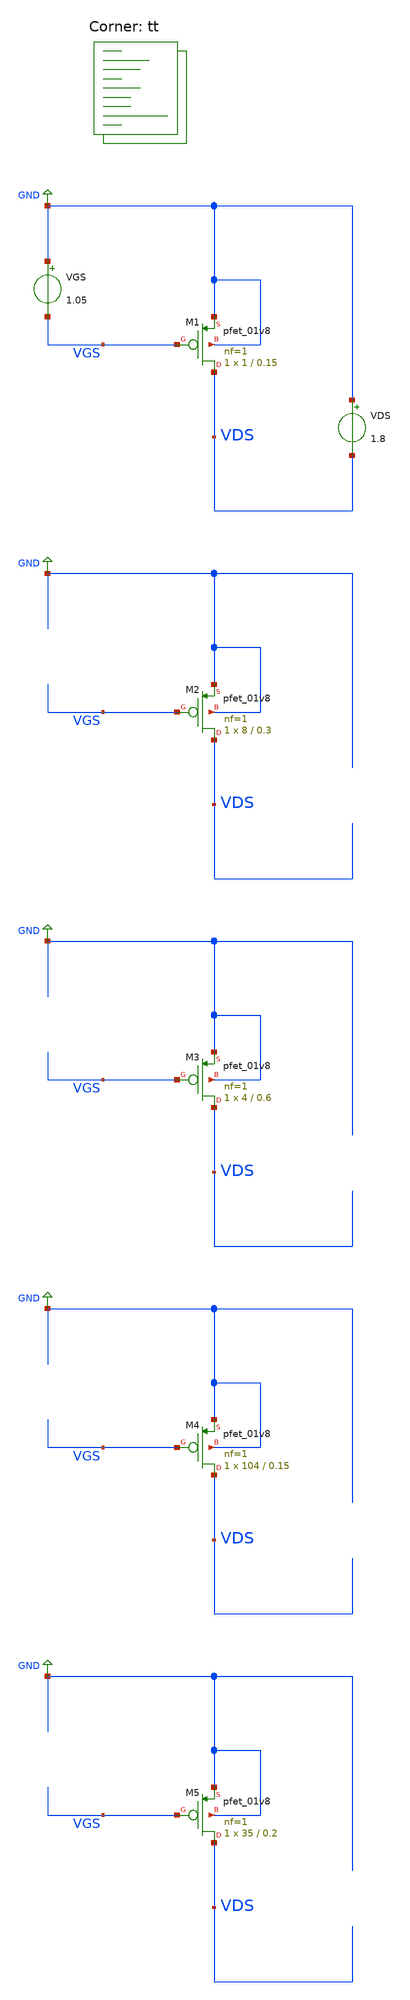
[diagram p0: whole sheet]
** sch_path: projects/opamp/xschem_ngspice/vds_vgs_sweep_pfet.sch
**.subckt vds_vgs_sweep_pfet
VGS GND VGS 1.05
VDS GND VDS 1.8
XM1 VDS VGS GND GND sky130_fd_pr__pfet_01v8 L=0.15 W=1 nf=1 ad='int((nf+1)/2) * W/nf * 0.29' as='int((nf+2)/2) * W/nf * 0.29'
+ pd='2*int((nf+1)/2) * (W/nf + 0.29)' ps='2*int((nf+2)/2) * (W/nf + 0.29)' nrd='0.29 / W' nrs='0.29 / W'
+ sa=0 sb=0 sd=0 mult=1 m=1
XM3 VDS VGS GND GND sky130_fd_pr__pfet_01v8 L=0.6 W=4 nf=1 ad='int((nf+1)/2) * W/nf * 0.29' as='int((nf+2)/2) * W/nf * 0.29'
+ pd='2*int((nf+1)/2) * (W/nf + 0.29)' ps='2*int((nf+2)/2) * (W/nf + 0.29)' nrd='0.29 / W' nrs='0.29 / W'
+ sa=0 sb=0 sd=0 mult=1 m=1
XM2 VDS VGS GND GND sky130_fd_pr__pfet_01v8 L=0.3 W=8 nf=1 ad='int((nf+1)/2) * W/nf * 0.29' as='int((nf+2)/2) * W/nf * 0.29'
+ pd='2*int((nf+1)/2) * (W/nf + 0.29)' ps='2*int((nf+2)/2) * (W/nf + 0.29)' nrd='0.29 / W' nrs='0.29 / W'
+ sa=0 sb=0 sd=0 mult=1 m=1
XM4 VDS VGS GND GND sky130_fd_pr__pfet_01v8 L=0.15 W=104 nf=1 ad='int((nf+1)/2) * W/nf * 0.29' as='int((nf+2)/2) * W/nf * 0.29'
+ pd='2*int((nf+1)/2) * (W/nf + 0.29)' ps='2*int((nf+2)/2) * (W/nf + 0.29)' nrd='0.29 / W' nrs='0.29 / W'
+ sa=0 sb=0 sd=0 mult=1 m=1
XM5 VDS VGS GND GND sky130_fd_pr__pfet_01v8 L=0.2 W=35 nf=1 ad='int((nf+1)/2) * W/nf * 0.29' as='int((nf+2)/2) * W/nf * 0.29'
+ pd='2*int((nf+1)/2) * (W/nf + 0.29)' ps='2*int((nf+2)/2) * (W/nf + 0.29)' nrd='0.29 / W' nrs='0.29 / W'
+ sa=0 sb=0 sd=0 mult=1 m=1
**** begin user architecture code
.lib $::SKYWATER_MODELS/sky130.lib.spice tt



.option method=gear
.option wnflag=1
.option savecurrents
*.temp = 120

.save @m.xm1.msky130_fd_pr__pfet_01v8[gm] @m.xm2.msky130_fd_pr__pfet_01v8[gm] @m.xm3.msky130_fd_pr__pfet_01v8[gm] @m.xm4.msky130_fd_pr__pfet_01v8[gm] @m.xm5.msky130_fd_pr__pfet_01v8[gm] @m.xm6.msky130_fd_pr__pfet_01v8[gm] @m.xm7.msky130_fd_pr__pfet_01v8[gm] @m.xm8.msky130_fd_pr__pfet_01v8[gm] @m.xm9.msky130_fd_pr__pfet_01v8[gm] @m.xm10.msky130_fd_pr__pfet_01v8[gm] @m.xm1.msky130_fd_pr__pfet_01v8[gds] @m.xm2.msky130_fd_pr__pfet_01v8[gds] @m.xm2.msky130_fd_pr__pfet_01v8[vth] @m.xm3.msky130_fd_pr__pfet_01v8[gds] @m.xm4.msky130_fd_pr__pfet_01v8[gds] @m.xm5.msky130_fd_pr__pfet_01v8[gds] @m.xm6.msky130_fd_pr__pfet_01v8[gds] @m.xm7.msky130_fd_pr__pfet_01v8[gds]


.control
  save all
  * dc VGS 0 1.8 0.1 VDS 0 1.8 0.1
  * dc VDS 0 1.0 0.001 VGS 0.0 1.13 1.13
  dc VDS 0 0.6 0.001 VGS 0.8 1.1 0.01
  remzerovec
  write vds_vgs_sweep_pfet.raw
  set appendwrite
  let rout1 = deriv(vds)/deriv(@m.xm1.msky130_fd_pr__pfet_01v8[id])
  let rout2 = deriv(vds)/deriv(@m.xm2.msky130_fd_pr__pfet_01v8[id])
  let rout3 = deriv(vds)/deriv(@m.xm3.msky130_fd_pr__pfet_01v8[id])
  let rout4 = deriv(vds)/deriv(@m.xm4.msky130_fd_pr__pfet_01v8[id])
  let rout5 = deriv(vds)/deriv(@m.xm5.msky130_fd_pr__pfet_01v8[id])
  show
.endc



**** end user architecture code
**.ends
.GLOBAL GND
.end
